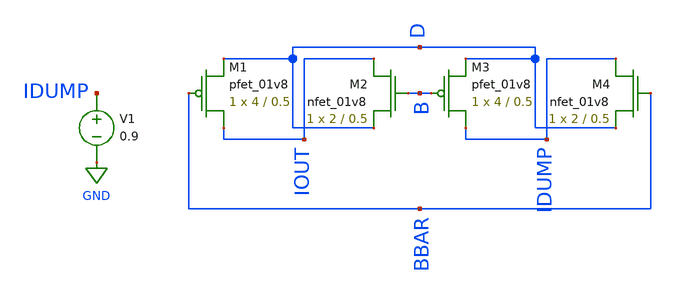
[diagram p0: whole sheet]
** sch_path: STEER.sch
**.subckt STEER
XM1 IOUT BBAR D VDD sky130_fd_pr__pfet_01v8 L=0.5 W=4 nf=1 ad='int((nf+1)/2) * W/nf * 0.29' as='int((nf+2)/2) * W/nf * 0.29'
+ pd='2*int((nf+1)/2) * (W/nf + 0.29)' ps='2*int((nf+2)/2) * (W/nf + 0.29)' nrd='0.29 / W' nrs='0.29 / W'
+ sa=0 sb=0 sd=0 mult=1 m=1
XM2 IOUT B D GND sky130_fd_pr__nfet_01v8 L=0.5 W=2 nf=1 ad='int((nf+1)/2) * W/nf * 0.29' as='int((nf+2)/2) * W/nf * 0.29'
+ pd='2*int((nf+1)/2) * (W/nf + 0.29)' ps='2*int((nf+2)/2) * (W/nf + 0.29)' nrd='0.29 / W' nrs='0.29 / W'
+ sa=0 sb=0 sd=0 mult=1 m=1
XM3 IDUMP B D VDD sky130_fd_pr__pfet_01v8 L=0.5 W=4 nf=1 ad='int((nf+1)/2) * W/nf * 0.29' as='int((nf+2)/2) * W/nf * 0.29'
+ pd='2*int((nf+1)/2) * (W/nf + 0.29)' ps='2*int((nf+2)/2) * (W/nf + 0.29)' nrd='0.29 / W' nrs='0.29 / W'
+ sa=0 sb=0 sd=0 mult=1 m=1
XM4 IDUMP BBAR D GND sky130_fd_pr__nfet_01v8 L=0.5 W=2 nf=1 ad='int((nf+1)/2) * W/nf * 0.29' as='int((nf+2)/2) * W/nf * 0.29'
+ pd='2*int((nf+1)/2) * (W/nf + 0.29)' ps='2*int((nf+2)/2) * (W/nf + 0.29)' nrd='0.29 / W' nrs='0.29 / W'
+ sa=0 sb=0 sd=0 mult=1 m=1
V1 IDUMP GND 0.9
**.ends
.GLOBAL GND
.end
